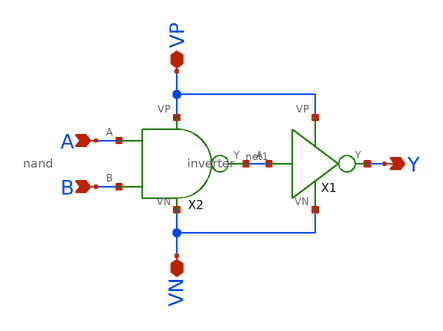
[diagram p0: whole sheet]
** sch_path: and_gate/schematics/and.sch
**.subckt and A B VN VP Y
*.ipin A
*.ipin B
*.iopin VN
*.iopin VP
*.opin Y
X1 net1 Y VP VN inverter
X2 A B net1 VN VP nand
**.ends
.end
